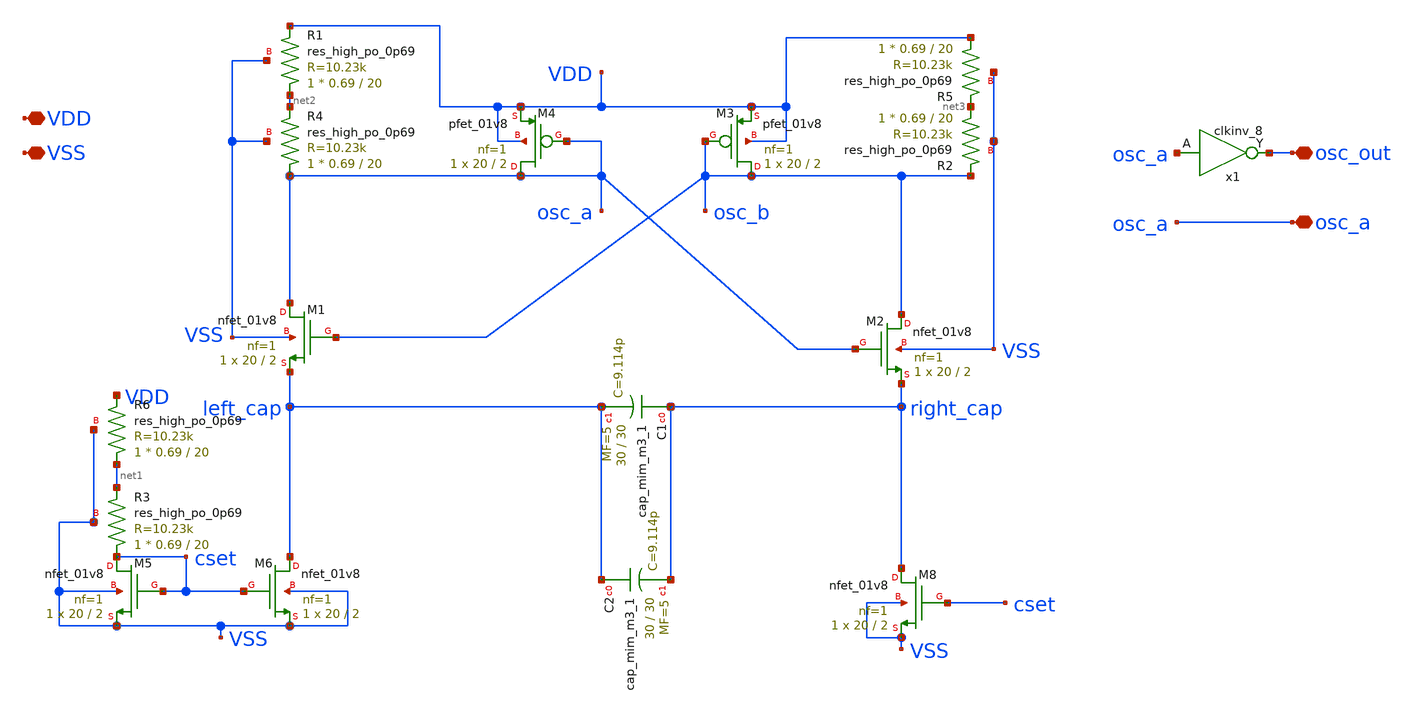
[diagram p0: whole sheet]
** sch_path: xschem/osc.sch
**.subckt osc osc_out VDD VSS osc_a
*.iopin osc_out
*.iopin VDD
*.iopin VSS
*.iopin osc_a
XM1 osc_a osc_b left_cap VSS sky130_fd_pr__nfet_01v8 L=2 W=20 nf=1 ad='int((nf+1)/2) * W/nf * 0.29' as='int((nf+2)/2) * W/nf * 0.29'
+ pd='2*int((nf+1)/2) * (W/nf + 0.29)' ps='2*int((nf+2)/2) * (W/nf + 0.29)' nrd='0.29 / W' nrs='0.29 / W'
+ sa=0 sb=0 sd=0 mult=1 m=1
XM2 osc_b osc_a right_cap VSS sky130_fd_pr__nfet_01v8 L=2 W=20 nf=1 ad='int((nf+1)/2) * W/nf * 0.29'
+ as='int((nf+2)/2) * W/nf * 0.29' pd='2*int((nf+1)/2) * (W/nf + 0.29)' ps='2*int((nf+2)/2) * (W/nf + 0.29)'
+ nrd='0.29 / W' nrs='0.29 / W' sa=0 sb=0 sd=0 mult=1 m=1
XM3 osc_b osc_b VDD VDD sky130_fd_pr__pfet_01v8 L=2 W=20 nf=1 ad='int((nf+1)/2) * W/nf * 0.29' as='int((nf+2)/2) * W/nf * 0.29'
+ pd='2*int((nf+1)/2) * (W/nf + 0.29)' ps='2*int((nf+2)/2) * (W/nf + 0.29)' nrd='0.29 / W' nrs='0.29 / W'
+ sa=0 sb=0 sd=0 mult=1 m=1
XM4 osc_a osc_a VDD VDD sky130_fd_pr__pfet_01v8 L=2 W=20 nf=1 ad='int((nf+1)/2) * W/nf * 0.29' as='int((nf+2)/2) * W/nf * 0.29'
+ pd='2*int((nf+1)/2) * (W/nf + 0.29)' ps='2*int((nf+2)/2) * (W/nf + 0.29)' nrd='0.29 / W' nrs='0.29 / W'
+ sa=0 sb=0 sd=0 mult=1 m=1
XC1 right_cap left_cap sky130_fd_pr__cap_mim_m3_1 W=30 L=30 MF=5 m=5
XM5 cset cset VSS VSS sky130_fd_pr__nfet_01v8 L=2 W=20 nf=1 ad='int((nf+1)/2) * W/nf * 0.29' as='int((nf+2)/2) * W/nf * 0.29'
+ pd='2*int((nf+1)/2) * (W/nf + 0.29)' ps='2*int((nf+2)/2) * (W/nf + 0.29)' nrd='0.29 / W' nrs='0.29 / W'
+ sa=0 sb=0 sd=0 mult=1 m=1
XM6 left_cap cset VSS VSS sky130_fd_pr__nfet_01v8 L=2 W=20 nf=1 ad='int((nf+1)/2) * W/nf * 0.29' as='int((nf+2)/2) * W/nf * 0.29'
+ pd='2*int((nf+1)/2) * (W/nf + 0.29)' ps='2*int((nf+2)/2) * (W/nf + 0.29)' nrd='0.29 / W' nrs='0.29 / W'
+ sa=0 sb=0 sd=0 mult=1 m=1
XM8 right_cap cset VSS VSS sky130_fd_pr__nfet_01v8 L=2 W=20 nf=1 ad='int((nf+1)/2) * W/nf * 0.29' as='int((nf+2)/2) * W/nf * 0.29'
+ pd='2*int((nf+1)/2) * (W/nf + 0.29)' ps='2*int((nf+2)/2) * (W/nf + 0.29)' nrd='0.29 / W' nrs='0.29 / W'
+ sa=0 sb=0 sd=0 mult=1 m=1
x1 osc_a VSS VSS VDD VDD osc_out sky130_fd_sc_hd__clkinv_8
XC2 left_cap right_cap sky130_fd_pr__cap_mim_m3_1 W=30 L=30 MF=5 m=5
XR4 osc_a net2 VSS sky130_fd_pr__res_high_po_0p69 L=20 mult=1 m=1
XR1 net2 VDD VSS sky130_fd_pr__res_high_po_0p69 L=20 mult=1 m=1
XR3 cset net1 VSS sky130_fd_pr__res_high_po_0p69 L=20 mult=1 m=1
XR2 net3 osc_b VSS sky130_fd_pr__res_high_po_0p69 L=20 mult=1 m=1
XR5 VDD net3 VSS sky130_fd_pr__res_high_po_0p69 L=20 mult=1 m=1
XR6 net1 VDD VSS sky130_fd_pr__res_high_po_0p69 L=20 mult=1 m=1
**.ends
.end
